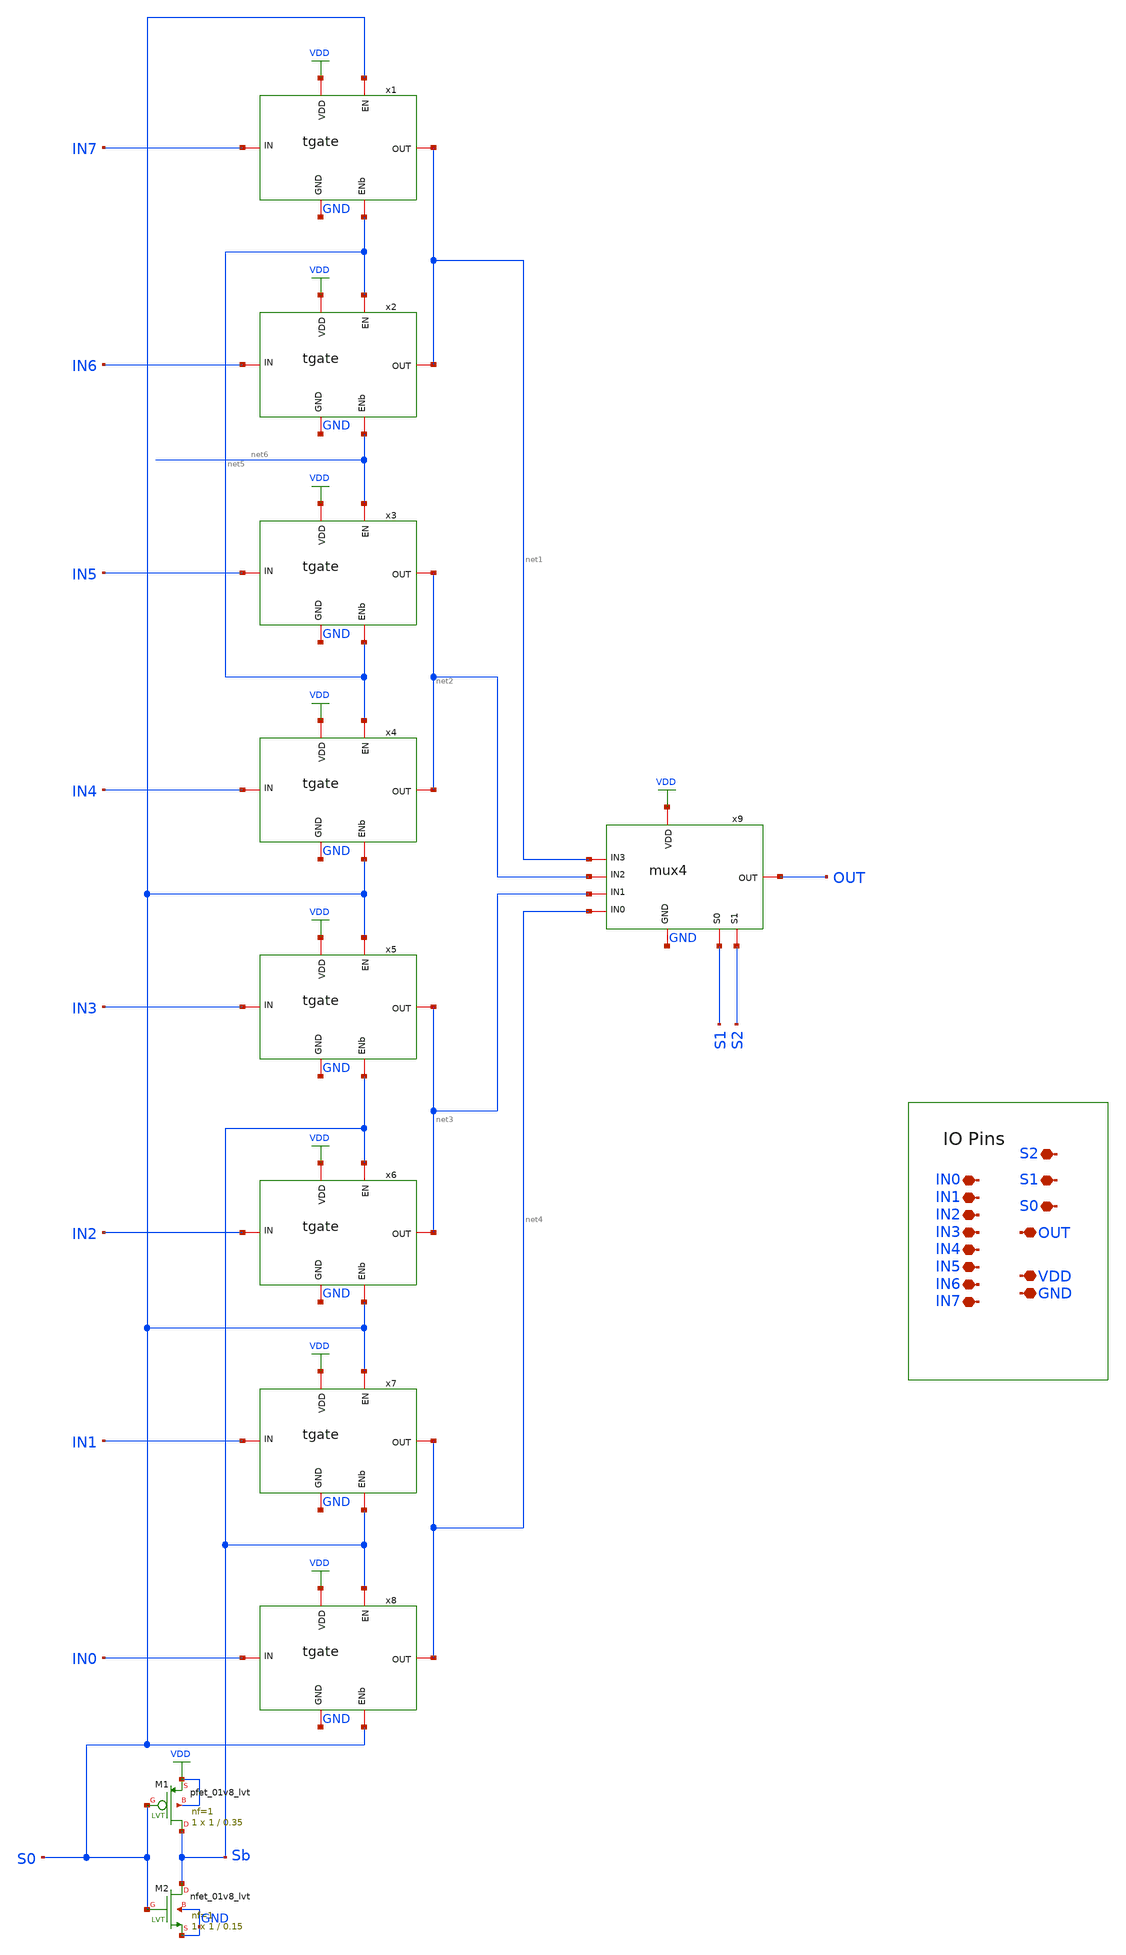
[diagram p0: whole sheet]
** sch_path: scope_sky130_v1/mux8.sch
**.subckt mux8 IN3 VDD GND S0 OUT IN2 IN1 IN0 S1 IN7 IN6 IN5 IN4 S2
*.iopin IN3
*.iopin VDD
*.iopin GND
*.iopin S0
*.iopin OUT
*.iopin IN2
*.iopin IN1
*.iopin IN0
*.iopin S1
*.iopin IN7
*.iopin IN6
*.iopin IN5
*.iopin IN4
*.iopin S2
XM1 Sb S0 VDD VDD sky130_fd_pr__pfet_01v8_lvt L=0.35 W=1 nf=1 ad='int((1 + 1)/2) * 1 / 1 * 0.29' as='int((1 + 2)/2) * 1 / 1 * 0.29'
+ pd='2*int((1 + 1)/2) * (1 / 1 + 0.29)' ps='2*int((1 + 2)/2) * (1 / 1 + 0.29)' nrd='0.29 / 1 ' nrs='0.29 / 1 '
+ sa=0 sb=0 sd=0 mult=1 m=1
XM2 Sb S0 GND GND sky130_fd_pr__nfet_01v8_lvt L=0.15 W=1 nf=1 ad='int((1 + 1)/2) * 1 / 1 * 0.29' as='int((1 + 2)/2) * 1 / 1 * 0.29'
+ pd='2*int((1 + 1)/2) * (1 / 1 + 0.29)' ps='2*int((1 + 2)/2) * (1 / 1 + 0.29)' nrd='0.29 / 1 ' nrs='0.29 / 1 '
+ sa=0 sb=0 sd=0 mult=1 m=1
x1 IN7 net1 net5 S0 VDD GND tgate
x2 IN6 net1 net6 net5 VDD GND tgate
x3 IN5 net2 net5 net6 VDD GND tgate
x4 IN4 net2 S0 net5 VDD GND tgate
x5 IN3 net3 Sb S0 VDD GND tgate
x6 IN2 net3 S0 Sb VDD GND tgate
x7 IN1 net4 Sb S0 VDD GND tgate
x8 IN0 net4 S0 Sb VDD GND tgate
x9 net2 net1 S1 S2 net4 net3 OUT VDD GND mux4
**.ends

* expanding   symbol:  scope_sky130_v1/tgate.sym # of pins=6
** sym_path: scope_sky130_v1/tgate.sym
** sch_path: scope_sky130_v1/tgate.sch
.subckt tgate IN OUT ENb EN VDD GND
*.iopin IN
*.iopin VDD
*.iopin GND
*.iopin ENb
*.iopin EN
*.iopin OUT
XM2 IN EN OUT GND sky130_fd_pr__nfet_01v8 L=0.15 W=0.5 nf=1 ad='int((1 + 1)/2) * 0.5 / 1 * 0.29' as='int((1 + 2)/2) * 0.5 / 1 * 0.29'
+ pd='2*int((1 + 1)/2) * (0.5 / 1 + 0.29)' ps='2*int((1 + 2)/2) * (0.5 / 1 + 0.29)' nrd='0.29 / 0.5 ' nrs='0.29 / 0.5 '
+ sa=0 sb=0 sd=0 mult=1 m=1
XM11 IN ENb OUT VDD sky130_fd_pr__pfet_01v8 L=0.15 W=0.5 nf=1 ad='int((nf+1)/2) * W/nf * 0.29' as='int((nf+2)/2) * W/nf * 0.29'
+ pd='2*int((nf+1)/2) * (W/nf + 0.29)' ps='2*int((nf+2)/2) * (W/nf + 0.29)' nrd='0.29 / W' nrs='0.29 / W'
+ sa=0 sb=0 sd=0 mult=1 m=1
.ends


* expanding   symbol:  scope_sky130_v1/mux4.sym # of pins=9
** sym_path: scope_sky130_v1/mux4.sym
** sch_path: scope_sky130_v1/mux4.sch
.subckt mux4 IN2 IN3 S0 S1 IN0 IN1 OUT VDD GND
*.iopin IN3
*.iopin VDD
*.iopin GND
*.iopin S0
*.iopin OUT
*.iopin IN2
*.iopin IN1
*.iopin IN0
*.iopin S1
XM1 Sb S0 VDD VDD sky130_fd_pr__pfet_01v8_lvt L=0.35 W=1 nf=1 ad='int((1 + 1)/2) * 1 / 1 * 0.29' as='int((1 + 2)/2) * 1 / 1 * 0.29'
+ pd='2*int((1 + 1)/2) * (1 / 1 + 0.29)' ps='2*int((1 + 2)/2) * (1 / 1 + 0.29)' nrd='0.29 / 1 ' nrs='0.29 / 1 '
+ sa=0 sb=0 sd=0 mult=1 m=1
XM2 Sb S0 GND GND sky130_fd_pr__nfet_01v8_lvt L=0.15 W=1 nf=1 ad='int((1 + 1)/2) * 1 / 1 * 0.29' as='int((1 + 2)/2) * 1 / 1 * 0.29'
+ pd='2*int((1 + 1)/2) * (1 / 1 + 0.29)' ps='2*int((1 + 2)/2) * (1 / 1 + 0.29)' nrd='0.29 / 1 ' nrs='0.29 / 1 '
+ sa=0 sb=0 sd=0 mult=1 m=1
x1 IN3 net1 Sb S0 VDD GND tgate
x2 IN2 net1 S0 Sb VDD GND tgate
x3 IN1 net2 Sb S0 VDD GND tgate
x4 IN0 net2 S0 Sb VDD GND tgate
x5 net2 net1 S1 OUT VDD GND mux2
.ends


* expanding   symbol:  scope_sky130_v1/mux2.sym # of pins=6
** sym_path: scope_sky130_v1/mux2.sym
** sch_path: scope_sky130_v1/mux2.sch
.subckt mux2 IN0 IN1 S OUT VDD GND
*.iopin IN1
*.iopin VDD
*.iopin GND
*.iopin S
*.iopin OUT
*.iopin IN0
XM1 Sb S VDD VDD sky130_fd_pr__pfet_01v8_lvt L=0.35 W=1 nf=1 ad='int((1 + 1)/2) * 1 / 1 * 0.29' as='int((1 + 2)/2) * 1 / 1 * 0.29'
+ pd='2*int((1 + 1)/2) * (1 / 1 + 0.29)' ps='2*int((1 + 2)/2) * (1 / 1 + 0.29)' nrd='0.29 / 1 ' nrs='0.29 / 1 '
+ sa=0 sb=0 sd=0 mult=1 m=1
XM2 Sb S GND GND sky130_fd_pr__nfet_01v8_lvt L=0.15 W=1 nf=1 ad='int((1 + 1)/2) * 1 / 1 * 0.29' as='int((1 + 2)/2) * 1 / 1 * 0.29'
+ pd='2*int((1 + 1)/2) * (1 / 1 + 0.29)' ps='2*int((1 + 2)/2) * (1 / 1 + 0.29)' nrd='0.29 / 1 ' nrs='0.29 / 1 '
+ sa=0 sb=0 sd=0 mult=1 m=1
x1 IN1 OUT Sb S VDD GND tgate
x2 IN0 OUT S Sb VDD GND tgate
.ends

.GLOBAL VDD
.end
